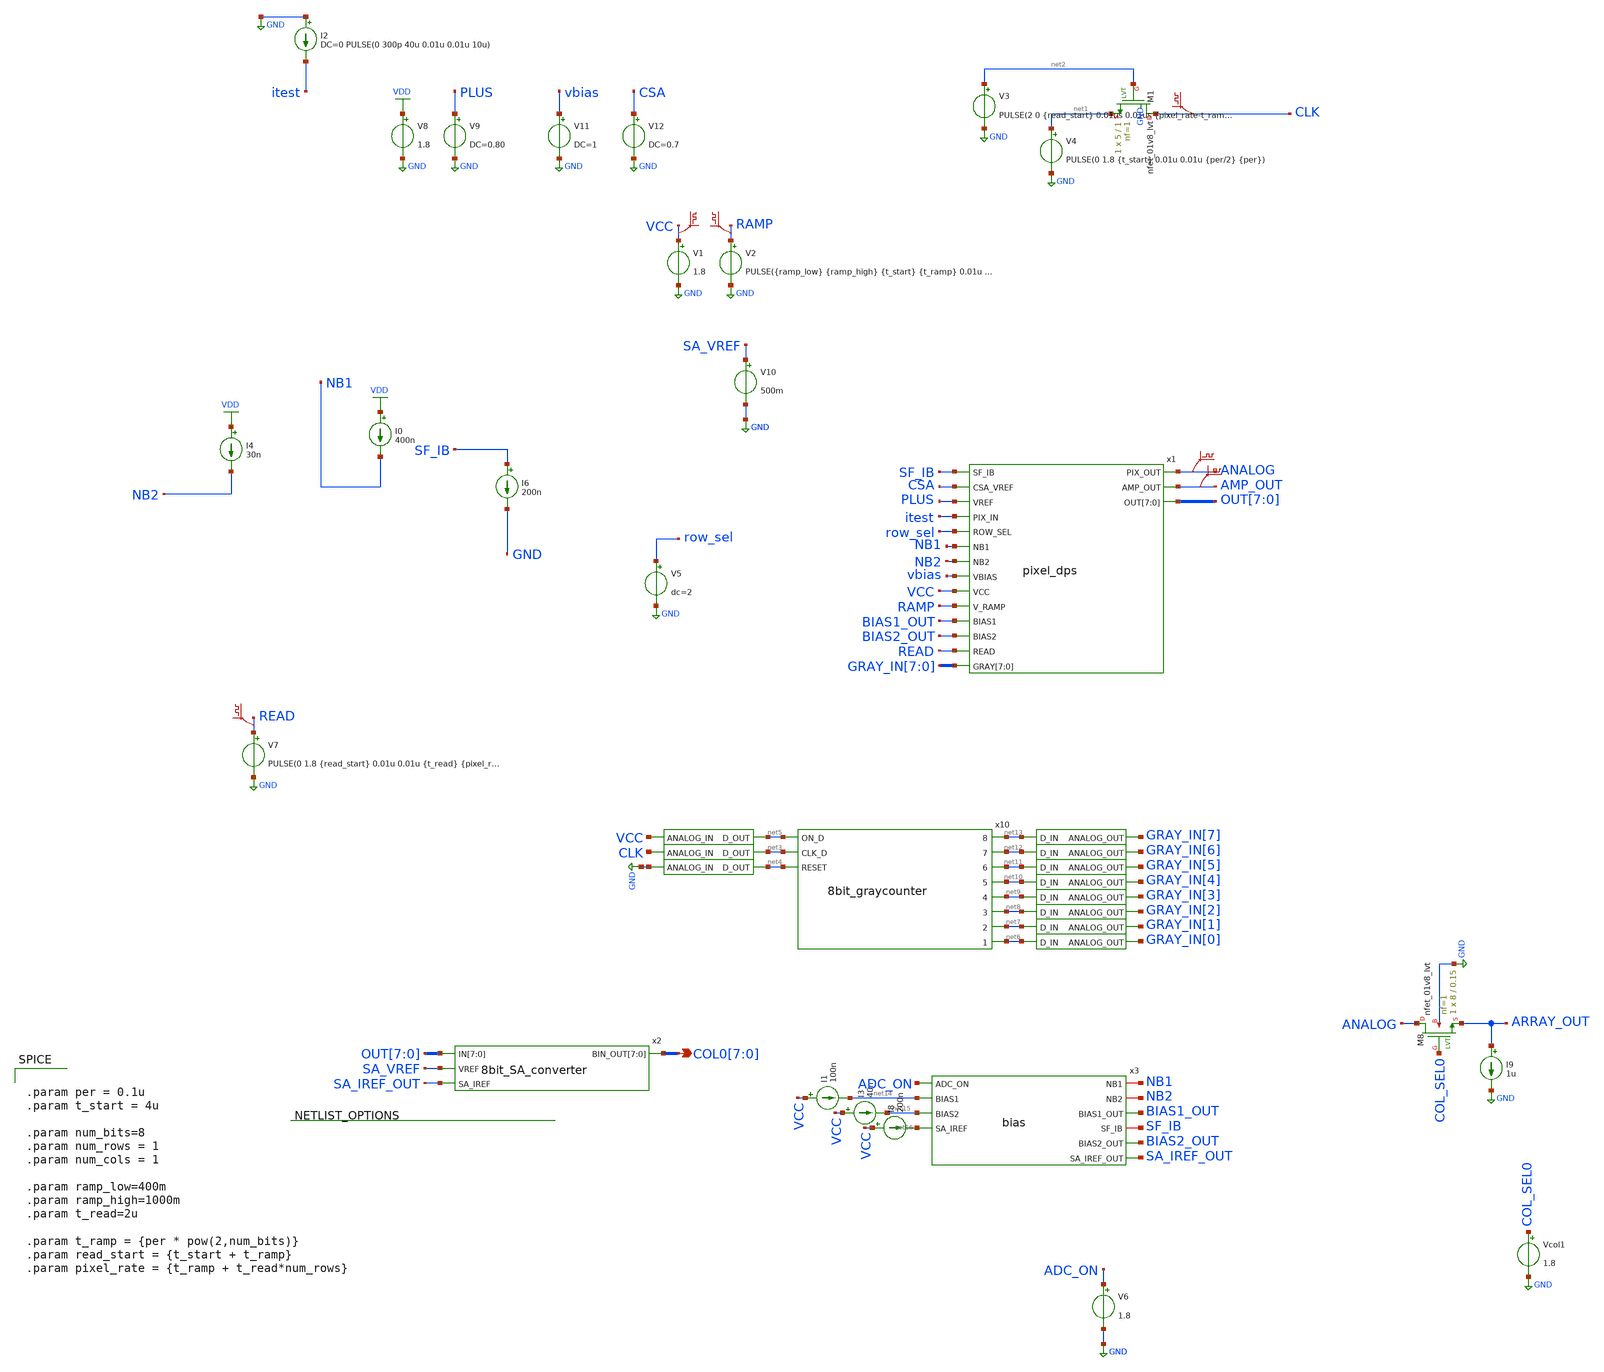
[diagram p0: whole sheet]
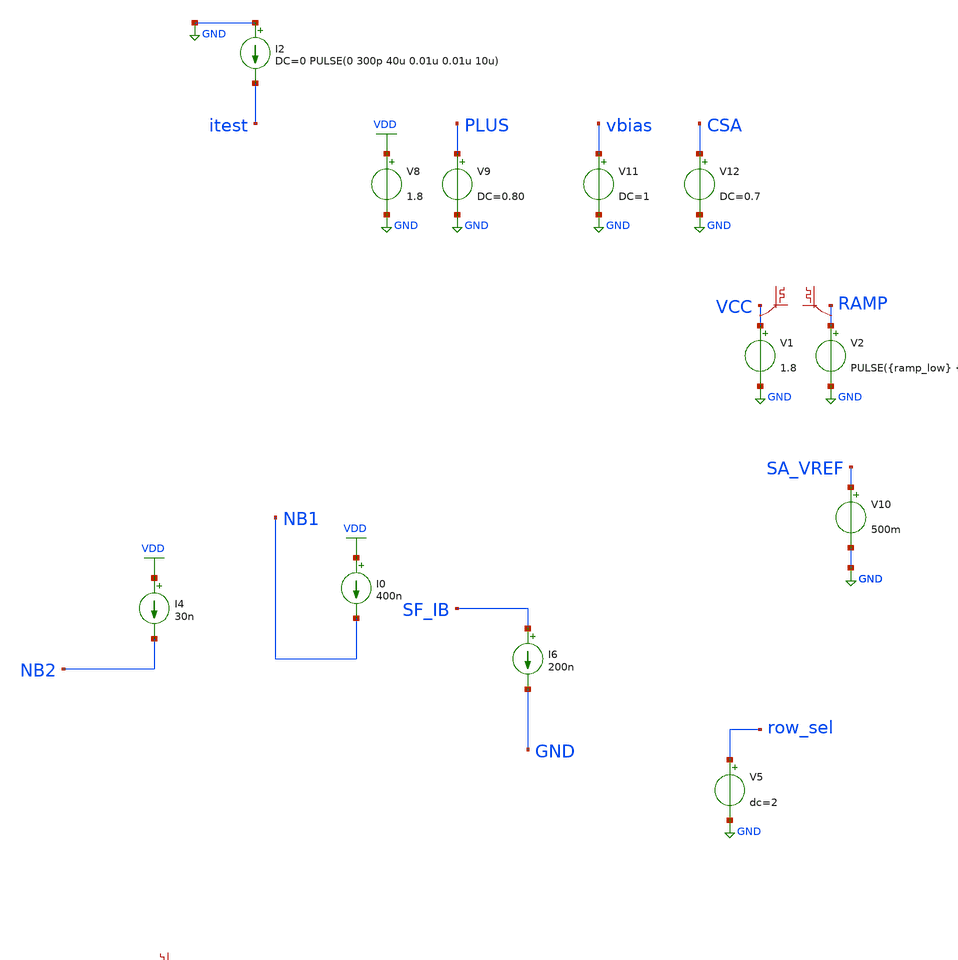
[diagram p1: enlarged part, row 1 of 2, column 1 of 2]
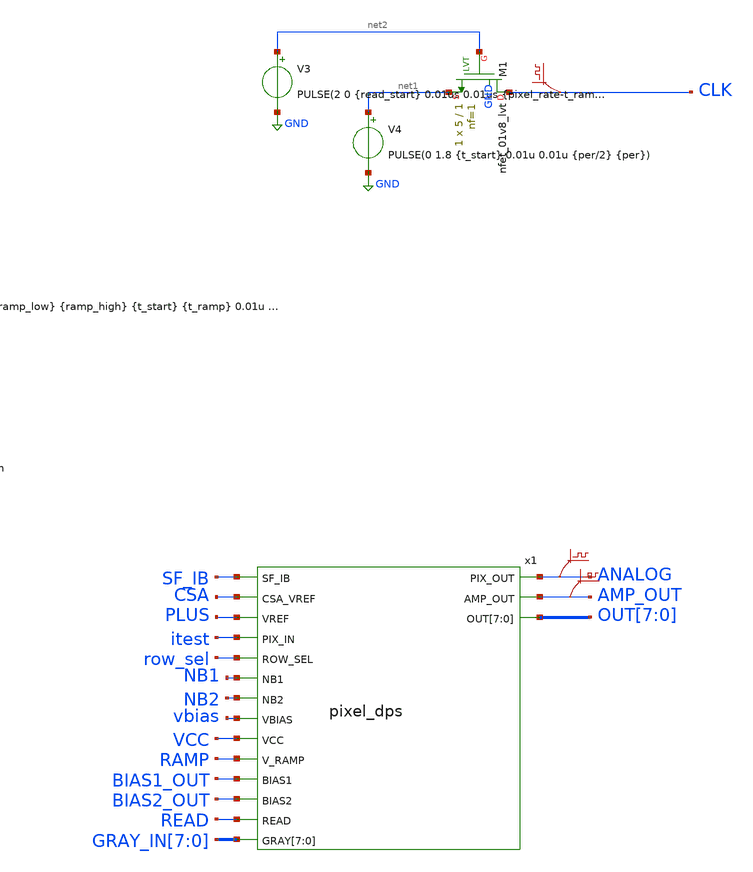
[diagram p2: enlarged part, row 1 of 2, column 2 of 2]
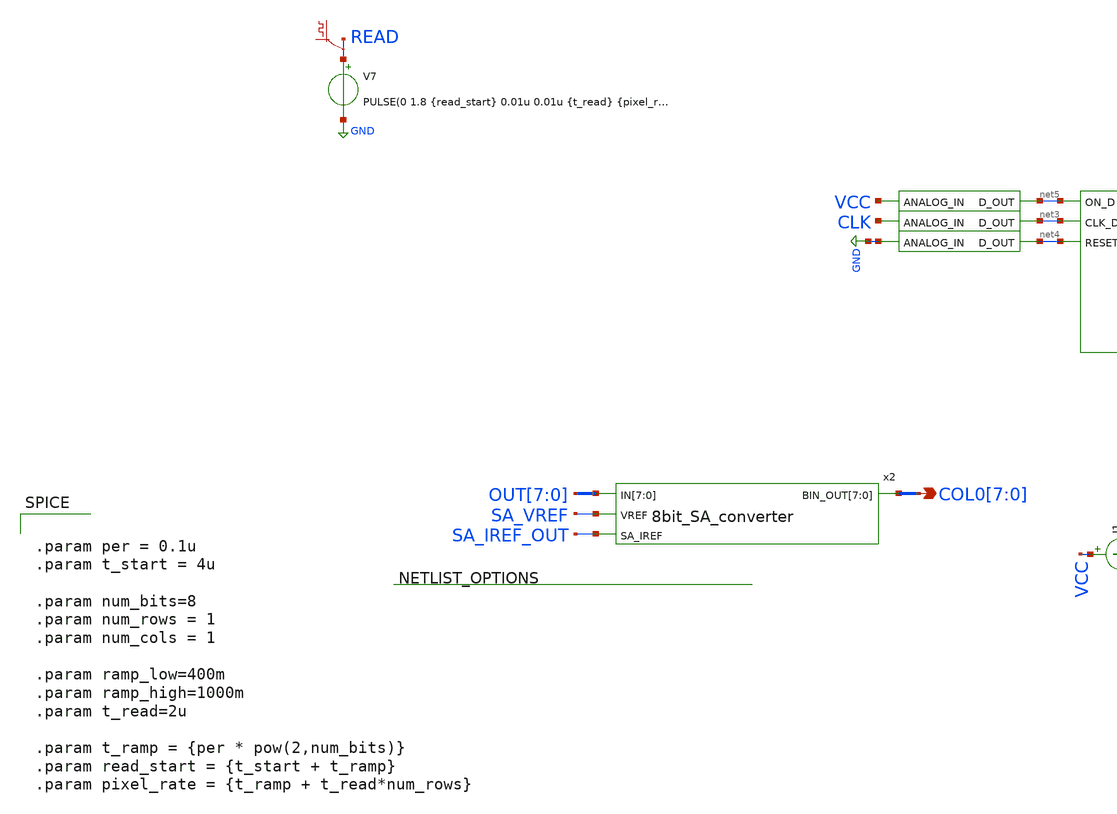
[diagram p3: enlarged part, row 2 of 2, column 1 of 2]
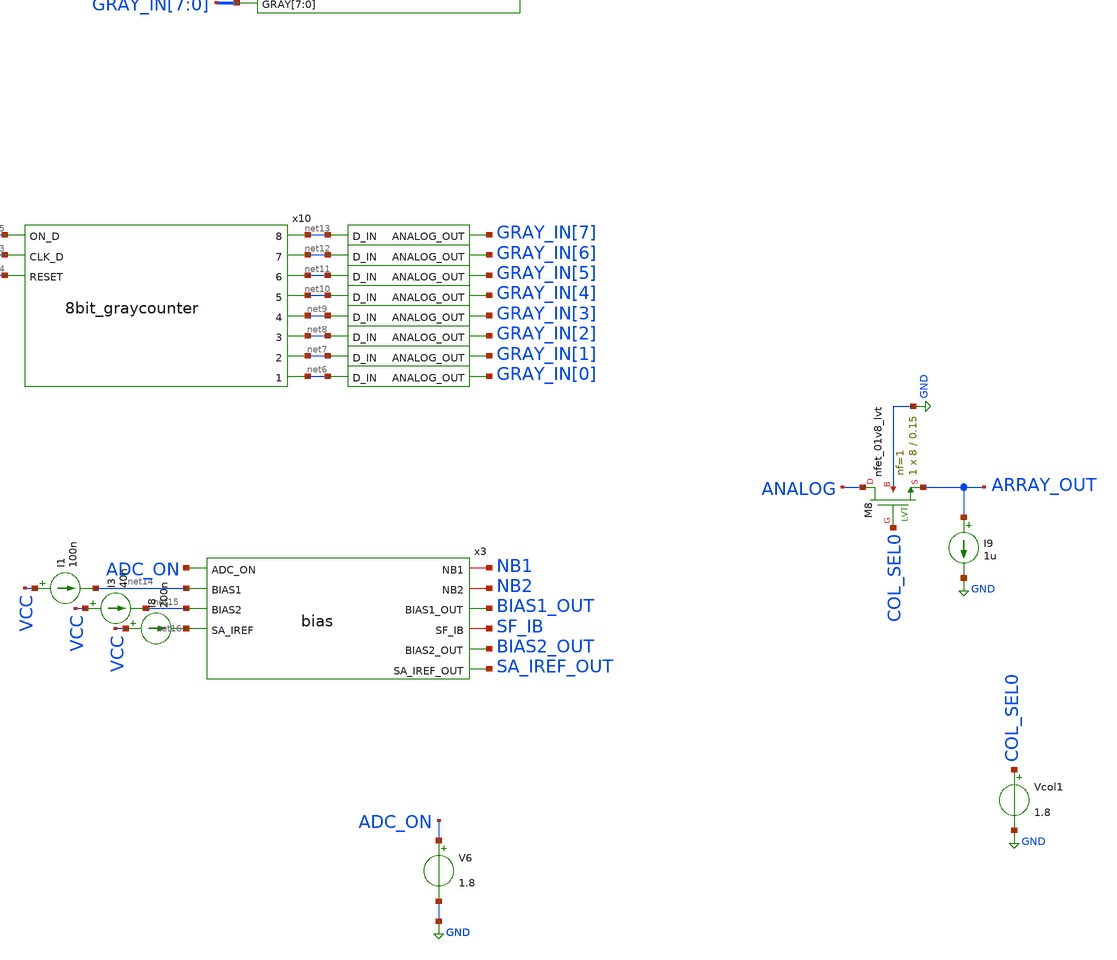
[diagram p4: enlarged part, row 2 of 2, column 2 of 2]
** sch_path: xschem/testbench/sim_dpspixel_tb.sch
**.subckt sim_dpspixel_tb COL0[7],COL0[6],COL0[5],COL0[4],COL0[3],COL0[2],COL0[1],COL0[0]
*.opin COL0[7],COL0[6],COL0[5],COL0[4],COL0[3],COL0[2],COL0[1],COL0[0]
x1 SF_IB CSA PLUS itest ANALOG AMP_OUT row_sel NB1 NB2 vbias OUT[7] OUT[6] OUT[5] OUT[4] OUT[3]
+ OUT[2] OUT[1] OUT[0] VCC RAMP BIAS1_OUT BIAS2_OUT READ GRAY_IN[7] GRAY_IN[6] GRAY_IN[5] GRAY_IN[4]
+ GRAY_IN[3] GRAY_IN[2] GRAY_IN[1] GRAY_IN[0] pixel_dps
I1 VCC net14 100n
I3 VCC net15 40n
V8 VDD GND 1.8
V9 PLUS GND DC=0.80
V11 vbias GND DC=1
V12 CSA GND DC=0.7
V1 VCC GND 1.8
V2 RAMP GND PULSE({ramp_low} {ramp_high} {t_start} {t_ramp} 0.01u {pixel_rate-t_ramp} {pixel_rate})
I0 VDD NB1 400n
I4 VDD NB2 30n
V10 SA_VREF GND 500m
I2 GND itest DC=0 PULSE(0 300p 40u 0.01u 0.01u 10u)
.save v(ramp)
.save v(vcc)
V4 net1 GND PULSE(0 1.8 {t_start} 0.01u 0.01u {per/2} {per})
V3 net2 GND PULSE(2 0 {read_start} 0.01us 0.01us {pixel_rate-t_ramp} {pixel_rate})
.save v(clk)
V7 READ GND PULSE(0 1.8 {read_start} 0.01u 0.01u {t_read} {pixel_rate})
.save v(read)
x2 OUT[7] OUT[6] OUT[5] OUT[4] OUT[3] OUT[2] OUT[1] OUT[0] SA_VREF SA_IREF_OUT COL0[7] COL0[6]
+ COL0[5] COL0[4] COL0[3] COL0[2] COL0[1] COL0[0] 8bit_SA_converter
x6 net4 GND adc_bridge
x8 net5 VCC adc_bridge
x7 net3 CLK adc_bridge
x10 net13 net5 net12 net3 net11 net10 net4 net9 net8 net7 net6 8bit_graycounter
x5 GRAY_IN[7] net13 dac_bridge
x9 GRAY_IN[6] net12 dac_bridge
x11 GRAY_IN[5] net11 dac_bridge
x12 GRAY_IN[4] net10 dac_bridge
x13 GRAY_IN[3] net9 dac_bridge
x14 GRAY_IN[2] net8 dac_bridge
x15 GRAY_IN[1] net7 dac_bridge
x16 GRAY_IN[0] net6 dac_bridge
.save v(analog)
I6 SF_IB GND 200n
V5 row_sel GND dc=2
.save v(amp_out)
I8 VCC net16 200n
XM8 ANALOG COL_SEL0 ARRAY_OUT GND sky130_fd_pr__nfet_01v8_lvt L=0.15 W=8 nf=1 ad='int((nf+1)/2) * W/nf * 0.29'
+ as='int((nf+2)/2) * W/nf * 0.29' pd='2*int((nf+1)/2) * (W/nf + 0.29)' ps='2*int((nf+2)/2) * (W/nf + 0.29)'
+ nrd='0.29 / W' nrs='0.29 / W' sa=0 sb=0 sd=0 mult=1 m=1
I9 ARRAY_OUT GND 1u
Vcol1 COL_SEL0 GND 1.8
x3 NB1 ADC_ON NB2 net14 BIAS1_OUT SF_IB net15 BIAS2_OUT net16 SA_IREF_OUT bias
V6 ADC_ON GND 1.8
XM1 CLK net2 net1 GND sky130_fd_pr__nfet_01v8_lvt L=1 W=5 nf=1 ad='int((nf+1)/2) * W/nf * 0.29' as='int((nf+2)/2) * W/nf * 0.29'
+ pd='2*int((nf+1)/2) * (W/nf + 0.29)' ps='2*int((nf+2)/2) * (W/nf + 0.29)' nrd='0.29 / W' nrs='0.29 / W'
+ sa=0 sb=0 sd=0 mult=1 m=1
**** begin user architecture code


.param per = 0.1u
.param t_start = 4u

.param num_bits=8
.param num_rows = 1
.param num_cols = 1

.param ramp_low=400m
.param ramp_high=1000m
.param t_read=2u

.param t_ramp = {per * pow(2,num_bits)}
.param read_start = {t_start + t_ramp}
.param pixel_rate = {t_ramp + t_read*num_rows}



** opencircuitdesign pdks install
.lib $::SKYWATER_MODELS/sky130.lib.spice tt


**** end user architecture code
**.ends
.GLOBAL GND
.GLOBAL VDD
**** begin user architecture code


.options gmin=10e-20
.control
save all

*dc v2 0 1.8 0.05
*plot v(test)
tran 1u 200u

write sim_dpspixel_tb.raw
.endc


**** end user architecture code
.end
